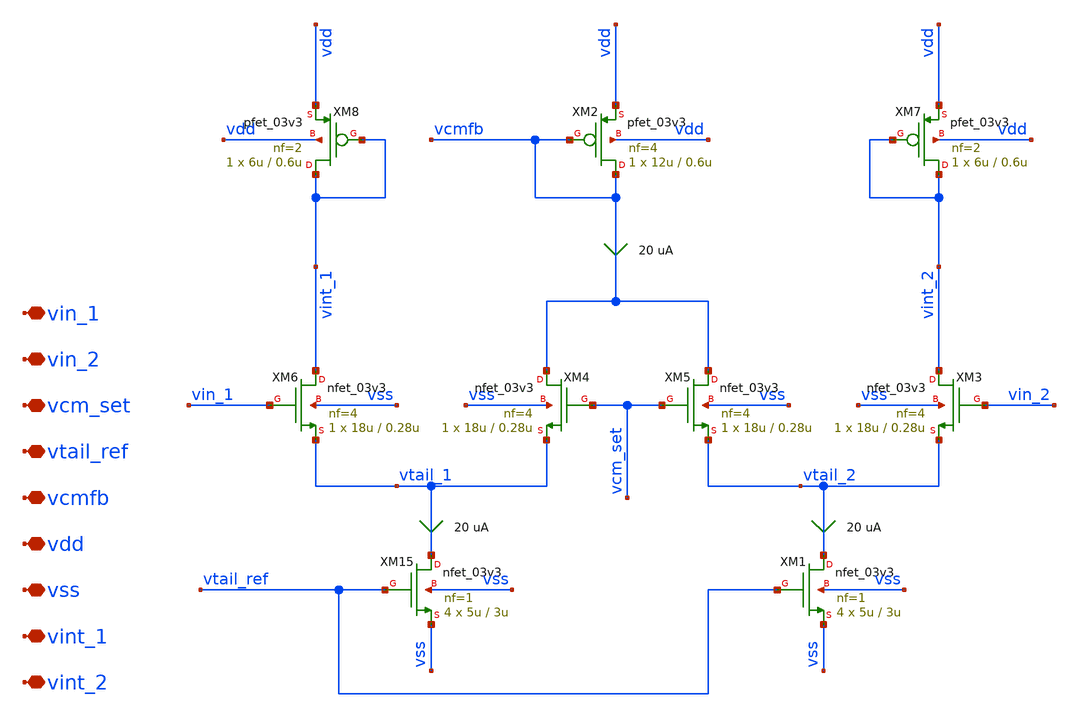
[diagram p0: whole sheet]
** sch_path: xschem/ccia_main_ota/b9_ccia_main_ota_s2_cmfb.sch
**.subckt b9_ccia_main_ota_s2_cmfb vin_1 vin_2 vcm_set vtail_ref vcmfb vdd vss vint_1 vint_2
*.iopin vin_1
*.iopin vin_2
*.iopin vcm_set
*.iopin vtail_ref
*.iopin vcmfb
*.iopin vdd
*.iopin vss
*.iopin vint_1
*.iopin vint_2
XM15 vtail_1 vtail_ref vss vss nfet_03v3 L=3u W=5u nf=1 ad='int((nf+1)/2) * W/nf * 0.18u' as='int((nf+2)/2) * W/nf * 0.18u'
+ pd='2*int((nf+1)/2) * (W/nf + 0.18u)' ps='2*int((nf+2)/2) * (W/nf + 0.18u)' nrd='0.18u / W' nrs='0.18u / W'
+ sa=0 sb=0 sd=0 m=4
XM1 vtail_2 vtail_ref vss vss nfet_03v3 L=3u W=5u nf=1 ad='int((nf+1)/2) * W/nf * 0.18u' as='int((nf+2)/2) * W/nf * 0.18u'
+ pd='2*int((nf+1)/2) * (W/nf + 0.18u)' ps='2*int((nf+2)/2) * (W/nf + 0.18u)' nrd='0.18u / W' nrs='0.18u / W'
+ sa=0 sb=0 sd=0 m=4
XM2 vcmfb vcmfb vdd vdd pfet_03v3 L=0.6u W=12u nf=4 ad='int((nf+1)/2) * W/nf * 0.18u' as='int((nf+2)/2) * W/nf * 0.18u'
+ pd='2*int((nf+1)/2) * (W/nf + 0.18u)' ps='2*int((nf+2)/2) * (W/nf + 0.18u)' nrd='0.18u / W' nrs='0.18u / W'
+ sa=0 sb=0 sd=0 m=1
XM7 vint_2 vint_2 vdd vdd pfet_03v3 L=0.6u W=6u nf=2 ad='int((nf+1)/2) * W/nf * 0.18u' as='int((nf+2)/2) * W/nf * 0.18u'
+ pd='2*int((nf+1)/2) * (W/nf + 0.18u)' ps='2*int((nf+2)/2) * (W/nf + 0.18u)' nrd='0.18u / W' nrs='0.18u / W'
+ sa=0 sb=0 sd=0 m=1
XM8 vint_1 vint_1 vdd vdd pfet_03v3 L=0.6u W=6u nf=2 ad='int((nf+1)/2) * W/nf * 0.18u' as='int((nf+2)/2) * W/nf * 0.18u'
+ pd='2*int((nf+1)/2) * (W/nf + 0.18u)' ps='2*int((nf+2)/2) * (W/nf + 0.18u)' nrd='0.18u / W' nrs='0.18u / W'
+ sa=0 sb=0 sd=0 m=1
XM4 vcmfb vcm_set vtail_1 vss nfet_03v3 L=0.28u W=18u nf=4 ad='int((nf+1)/2) * W/nf * 0.18u' as='int((nf+2)/2) * W/nf * 0.18u'
+ pd='2*int((nf+1)/2) * (W/nf + 0.18u)' ps='2*int((nf+2)/2) * (W/nf + 0.18u)' nrd='0.18u / W' nrs='0.18u / W'
+ sa=0 sb=0 sd=0 m=1
XM3 vint_2 vin_2 vtail_2 vss nfet_03v3 L=0.28u W=18u nf=4 ad='int((nf+1)/2) * W/nf * 0.18u' as='int((nf+2)/2) * W/nf * 0.18u'
+ pd='2*int((nf+1)/2) * (W/nf + 0.18u)' ps='2*int((nf+2)/2) * (W/nf + 0.18u)' nrd='0.18u / W' nrs='0.18u / W'
+ sa=0 sb=0 sd=0 m=1
XM5 vcmfb vcm_set vtail_2 vss nfet_03v3 L=0.28u W=18u nf=4 ad='int((nf+1)/2) * W/nf * 0.18u' as='int((nf+2)/2) * W/nf * 0.18u'
+ pd='2*int((nf+1)/2) * (W/nf + 0.18u)' ps='2*int((nf+2)/2) * (W/nf + 0.18u)' nrd='0.18u / W' nrs='0.18u / W'
+ sa=0 sb=0 sd=0 m=1
XM6 vint_1 vin_1 vtail_1 vss nfet_03v3 L=0.28u W=18u nf=4 ad='int((nf+1)/2) * W/nf * 0.18u' as='int((nf+2)/2) * W/nf * 0.18u'
+ pd='2*int((nf+1)/2) * (W/nf + 0.18u)' ps='2*int((nf+2)/2) * (W/nf + 0.18u)' nrd='0.18u / W' nrs='0.18u / W'
+ sa=0 sb=0 sd=0 m=1
**.ends
.end
